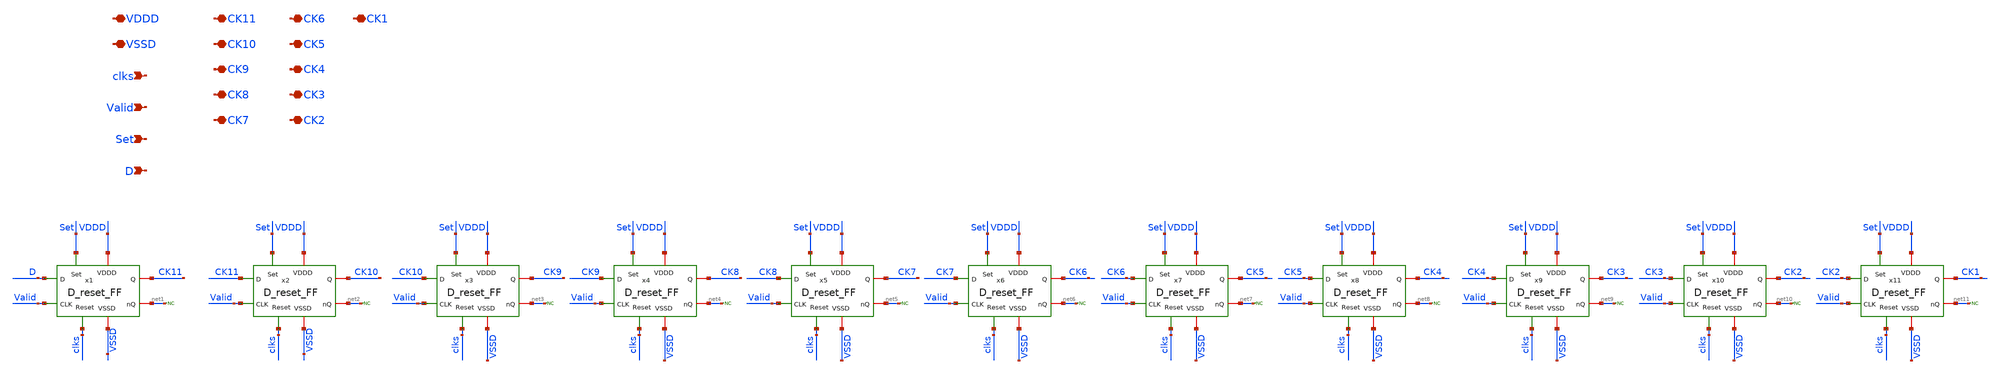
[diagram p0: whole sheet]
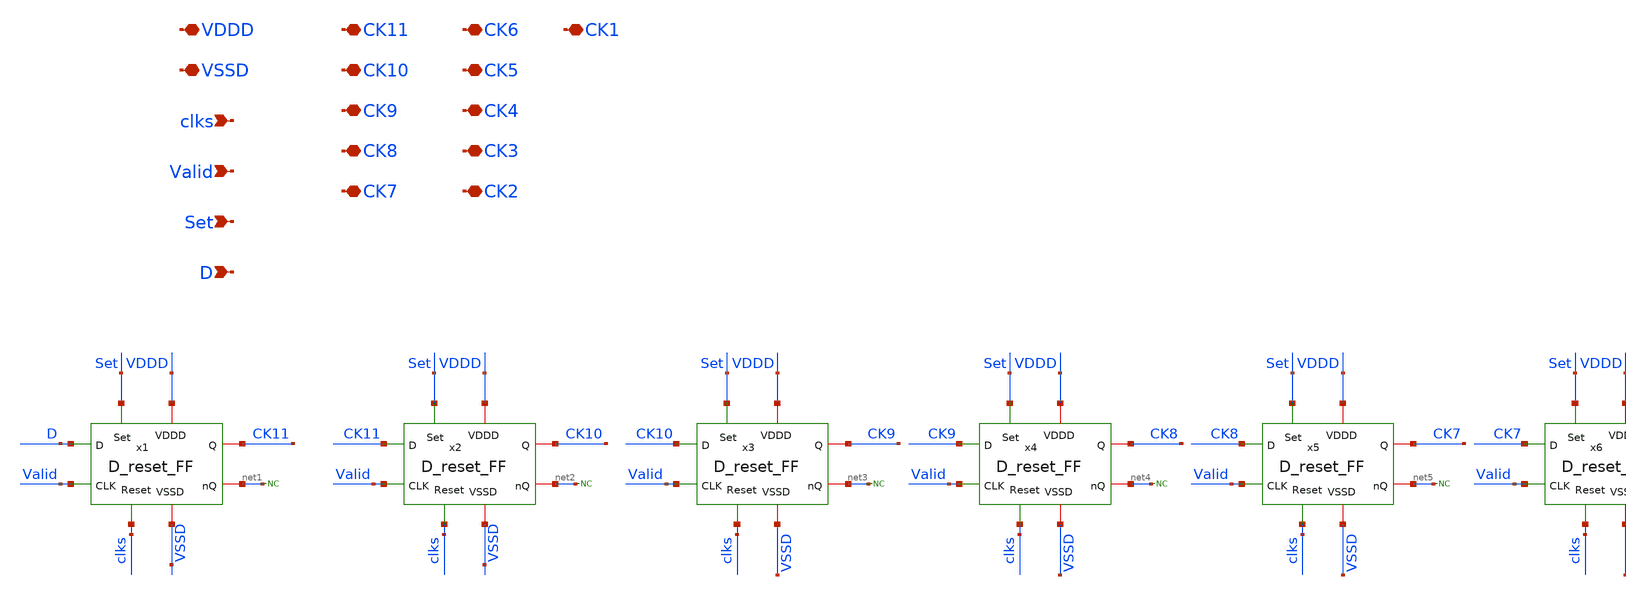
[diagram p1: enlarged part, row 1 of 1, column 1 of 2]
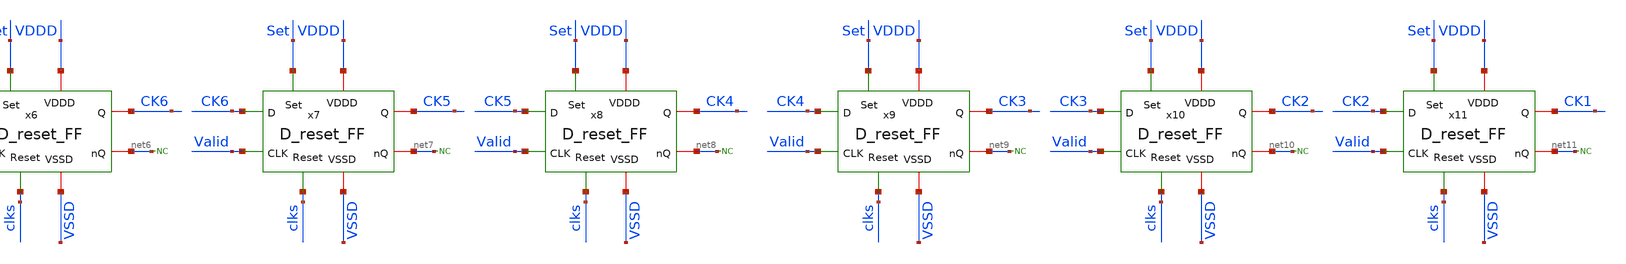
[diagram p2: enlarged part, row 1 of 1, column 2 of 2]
** sch_path: SAR_ADC/SAR_logic/xschem/SAR_Logic.sch
**.subckt SAR_Logic VDDD VSSD CK11 CK10 CK9 CK8 CK7 CK6 CK5 CK4 CK3 CK2 CK1 clks Valid Set D
*.iopin VDDD
*.iopin VSSD
*.iopin CK11
*.iopin CK10
*.iopin CK9
*.iopin CK8
*.iopin CK7
*.iopin CK6
*.iopin CK5
*.iopin CK4
*.iopin CK3
*.iopin CK2
*.iopin CK1
*.ipin clks
*.ipin Valid
*.ipin Set
*.ipin D
* noconn #net1
* noconn #net2
* noconn #net3
* noconn #net4
* noconn #net5
* noconn #net6
* noconn #net7
* noconn #net8
* noconn #net9
* noconn #net10
* noconn #net11
x1 VDDD CK11 Valid D net1 Set clks VSSD D_reset_FF
x2 VDDD CK10 Valid CK11 net2 Set clks VSSD D_reset_FF
x3 VDDD CK9 Valid CK10 net3 Set clks VSSD D_reset_FF
x4 VDDD CK8 Valid CK9 net4 Set clks VSSD D_reset_FF
x5 VDDD CK7 Valid CK8 net5 Set clks VSSD D_reset_FF
x6 VDDD CK6 Valid CK7 net6 Set clks VSSD D_reset_FF
x7 VDDD CK5 Valid CK6 net7 Set clks VSSD D_reset_FF
x8 VDDD CK4 Valid CK5 net8 Set clks VSSD D_reset_FF
x9 VDDD CK3 Valid CK4 net9 Set clks VSSD D_reset_FF
x10 VDDD CK2 Valid CK3 net10 Set clks VSSD D_reset_FF
x11 VDDD CK1 Valid CK2 net11 Set clks VSSD D_reset_FF
**.ends
.end
